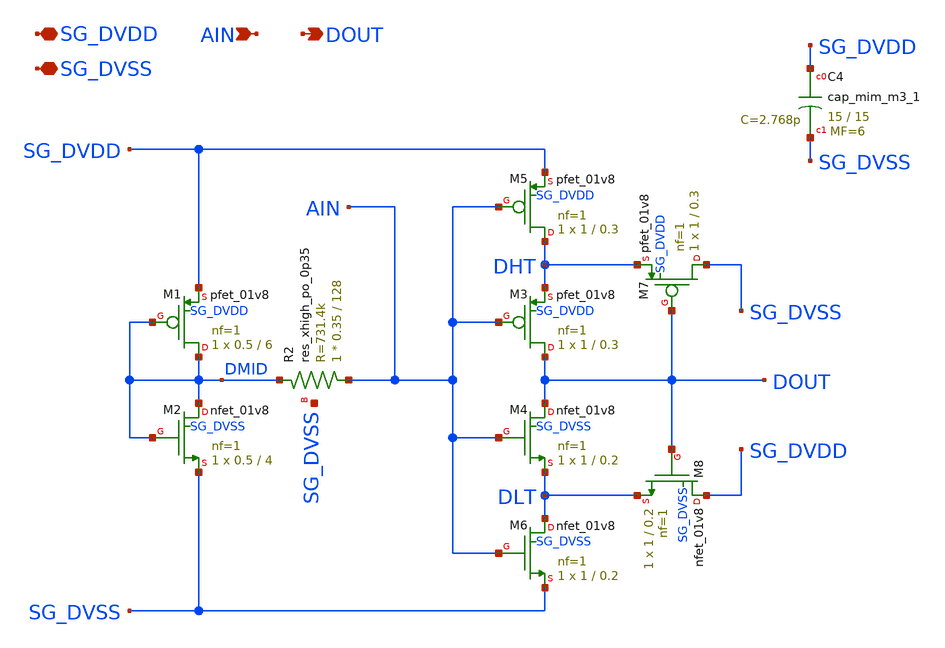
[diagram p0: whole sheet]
** sch_path: xschem/schmitt_trigger_pullmid.sch
**.subckt schmitt_trigger_pullmid SG_DVDD SG_DVSS AIN DOUT
*.iopin SG_DVDD
*.iopin SG_DVSS
*.ipin AIN
*.opin DOUT
XM1 DMID DMID SG_DVDD SG_DVDD sky130_fd_pr__pfet_01v8 L=6 W=0.5 nf=1 ad='int((1 + 1)/2) * 0.5 / 1 * 0.29'
+ as='int((1 + 2)/2) * 0.5 / 1 * 0.29' pd='2*int((1 + 1)/2) * (0.5 / 1 + 0.29)' ps='2*int((1 + 2)/2) * (0.5 / 1 + 0.29)'
+ nrd='0.29 / 0.5 ' nrs='0.29 / 0.5 ' sa=0 sb=0 sd=0 mult=1 m=1
XM2 DMID DMID SG_DVSS SG_DVSS sky130_fd_pr__nfet_01v8 L=4 W=0.5 nf=1 ad='int((nf+1)/2) * W/nf * 0.29'
+ as='int((nf+2)/2) * W/nf * 0.29' pd='2*int((nf+1)/2) * (W/nf + 0.29)' ps='2*int((nf+2)/2) * (W/nf + 0.29)'
+ nrd='0.29 / W' nrs='0.29 / W' sa=0 sb=0 sd=0 mult=1 m=1
XR2 AIN DMID SG_DVSS sky130_fd_pr__res_xhigh_po_0p35 L=128 mult=1 m=1
XM3 DOUT AIN DHT SG_DVDD sky130_fd_pr__pfet_01v8 L=0.3 W=1 nf=1 ad='int((1 + 1)/2) * 1 / 1 * 0.29' as='int((1 + 2)/2) * 1 / 1 * 0.29'
+ pd='2*int((1 + 1)/2) * (1 / 1 + 0.29)' ps='2*int((1 + 2)/2) * (1 / 1 + 0.29)' nrd='0.29 / 1 ' nrs='0.29 / 1 '
+ sa=0 sb=0 sd=0 mult=1 m=1
XM4 DOUT AIN DLT SG_DVSS sky130_fd_pr__nfet_01v8 L=0.2 W=1 nf=1 ad='int((nf+1)/2) * W/nf * 0.29' as='int((nf+2)/2) * W/nf * 0.29'
+ pd='2*int((nf+1)/2) * (W/nf + 0.29)' ps='2*int((nf+2)/2) * (W/nf + 0.29)' nrd='0.29 / W' nrs='0.29 / W'
+ sa=0 sb=0 sd=0 mult=1 m=1
XM5 DHT AIN SG_DVDD SG_DVDD sky130_fd_pr__pfet_01v8 L=0.3 W=1 nf=1 ad='int((1 + 1)/2) * 1 / 1 * 0.29'
+ as='int((1 + 2)/2) * 1 / 1 * 0.29' pd='2*int((1 + 1)/2) * (1 / 1 + 0.29)' ps='2*int((1 + 2)/2) * (1 / 1 + 0.29)'
+ nrd='0.29 / 1 ' nrs='0.29 / 1 ' sa=0 sb=0 sd=0 mult=1 m=1
XM6 DLT AIN SG_DVSS SG_DVSS sky130_fd_pr__nfet_01v8 L=0.2 W=1 nf=1 ad='int((nf+1)/2) * W/nf * 0.29' as='int((nf+2)/2) * W/nf * 0.29'
+ pd='2*int((nf+1)/2) * (W/nf + 0.29)' ps='2*int((nf+2)/2) * (W/nf + 0.29)' nrd='0.29 / W' nrs='0.29 / W'
+ sa=0 sb=0 sd=0 mult=1 m=1
XM7 SG_DVSS DOUT DHT SG_DVDD sky130_fd_pr__pfet_01v8 L=0.3 W=1 nf=1 ad='int((1 + 1)/2) * 1 / 1 * 0.29'
+ as='int((1 + 2)/2) * 1 / 1 * 0.29' pd='2*int((1 + 1)/2) * (1 / 1 + 0.29)' ps='2*int((1 + 2)/2) * (1 / 1 + 0.29)'
+ nrd='0.29 / 1 ' nrs='0.29 / 1 ' sa=0 sb=0 sd=0 mult=1 m=1
XM8 SG_DVDD DOUT DLT SG_DVSS sky130_fd_pr__nfet_01v8 L=0.2 W=1 nf=1 ad='int((nf+1)/2) * W/nf * 0.29'
+ as='int((nf+2)/2) * W/nf * 0.29' pd='2*int((nf+1)/2) * (W/nf + 0.29)' ps='2*int((nf+2)/2) * (W/nf + 0.29)'
+ nrd='0.29 / W' nrs='0.29 / W' sa=0 sb=0 sd=0 mult=1 m=1
XC4 SG_DVDD SG_DVSS sky130_fd_pr__cap_mim_m3_1 W=15 L=15 MF=6 m=6
**.ends
.end
